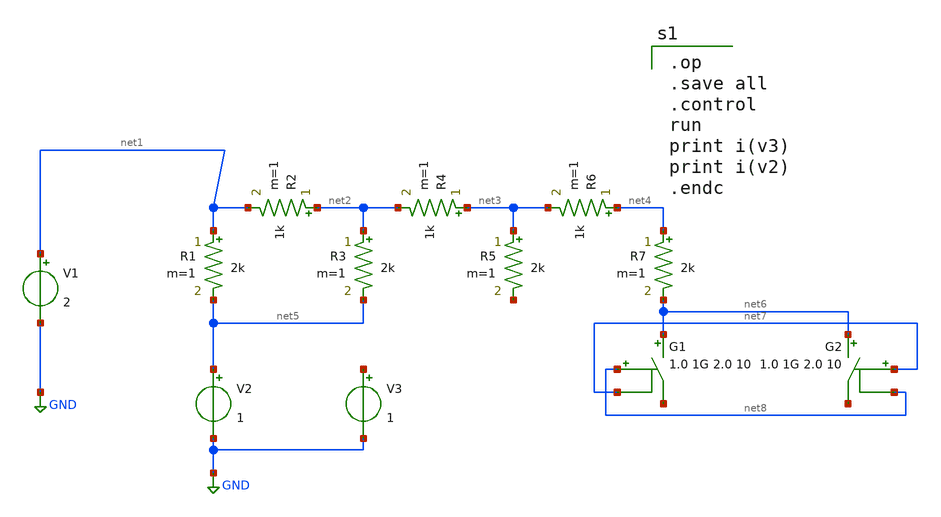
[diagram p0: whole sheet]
** sch_path: xschem/r2rtest.sch
**.subckt r2rtest
R1 net1 net5 2k m=1
R2 net2 net1 1k m=1
R3 net2 net5 2k m=1
R4 net3 net2 1k m=1
R5 net3 net9 2k m=1
R6 net4 net3 1k m=1
R7 net4 net6 2k m=1
V1 net1 GND 2
V2 net5 GND 1
V3 net10 GND 1
G1 net6 net11 vcr pwl(1) net8 net7 1.0 1G 2.0 10
G2 net6 net12 vcr pwl(1) net7 net8 1.0 1G 2.0 10
**** begin user architecture code

.op
.save all
.control
run
print i(v3)
print i(v2)
.endc

**** end user architecture code
**.ends
.GLOBAL GND
.end
